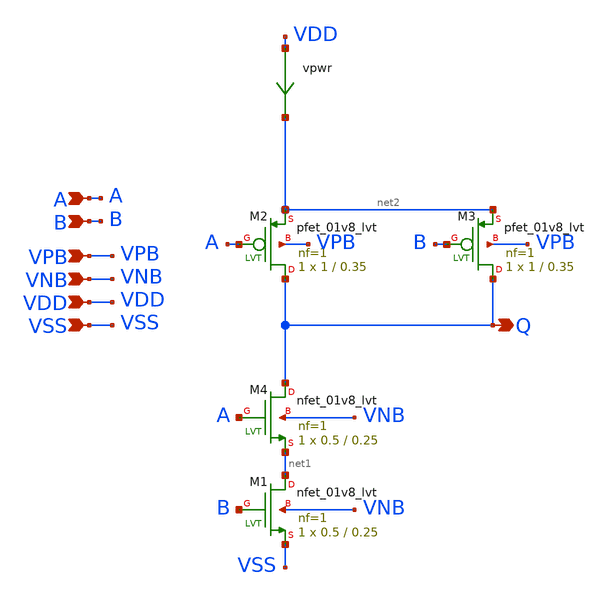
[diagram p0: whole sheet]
** sch_path: xschem/pll_nand.sch
**.subckt pll_nand Q A B VDD VPB VNB VSS
*.opin Q
*.ipin A
*.ipin B
*.ipin VDD
*.ipin VPB
*.ipin VNB
*.ipin VSS
XM3 Q B net2 VPB sky130_fd_pr__pfet_01v8_lvt L=0.35 W=1 nf=1 ad='int((nf+1)/2) * W/nf * 0.29' as='int((nf+2)/2) * W/nf * 0.29'
+ pd='2*int((nf+1)/2) * (W/nf + 0.29)' ps='2*int((nf+2)/2) * (W/nf + 0.29)' nrd='0.29 / W' nrs='0.29 / W'
+ sa=0 sb=0 sd=0 mult=1 m=1
vpwr VDD net2 0
.save i(vpwr)
XM1 net1 B VSS VNB sky130_fd_pr__nfet_01v8_lvt L=0.25 W=0.5 nf=1 ad='int((nf+1)/2) * W/nf * 0.29' as='int((nf+2)/2) * W/nf * 0.29'
+ pd='2*int((nf+1)/2) * (W/nf + 0.29)' ps='2*int((nf+2)/2) * (W/nf + 0.29)' nrd='0.29 / W' nrs='0.29 / W'
+ sa=0 sb=0 sd=0 mult=1 m=1
XM2 Q A net2 VPB sky130_fd_pr__pfet_01v8_lvt L=0.35 W=1 nf=1 ad='int((nf+1)/2) * W/nf * 0.29' as='int((nf+2)/2) * W/nf * 0.29'
+ pd='2*int((nf+1)/2) * (W/nf + 0.29)' ps='2*int((nf+2)/2) * (W/nf + 0.29)' nrd='0.29 / W' nrs='0.29 / W'
+ sa=0 sb=0 sd=0 mult=1 m=1
XM4 Q A net1 VNB sky130_fd_pr__nfet_01v8_lvt L=0.25 W=0.5 nf=1 ad='int((nf+1)/2) * W/nf * 0.29' as='int((nf+2)/2) * W/nf * 0.29'
+ pd='2*int((nf+1)/2) * (W/nf + 0.29)' ps='2*int((nf+2)/2) * (W/nf + 0.29)' nrd='0.29 / W' nrs='0.29 / W'
+ sa=0 sb=0 sd=0 mult=1 m=1
**.ends
.end
